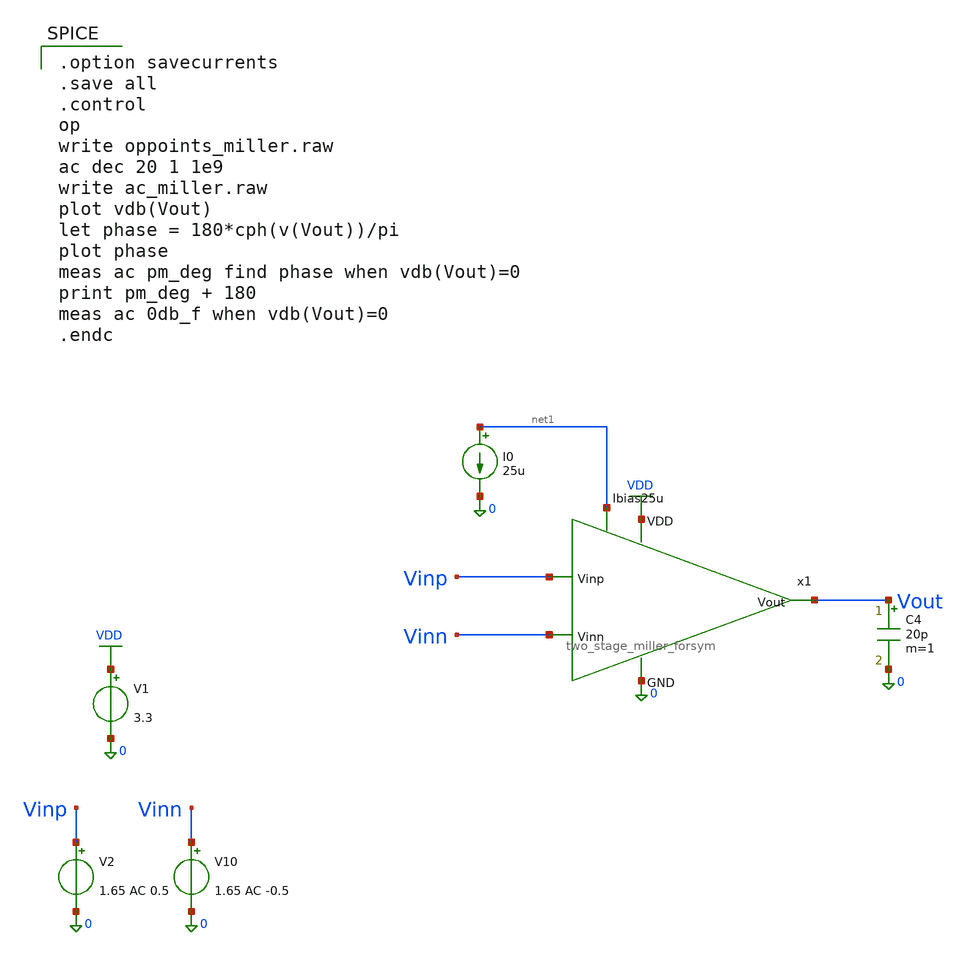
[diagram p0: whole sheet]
** sch_path: jz_tia/two_stage_miller_forsym_tb.sch
**.subckt two_stage_miller_forsym_tb
V2 Vinp 0 1.65 AC 0.5
V10 Vinn 0 1.65 AC -0.5
V1 VDD 0 3.3
I0 net1 0 25u
C4 Vout 0 20p m=1
x1 VDD Vout Vinp Vinn net1 0 two_stage_miller_forsym
**** begin user architecture code

.include $::180MCU_MODELS/design.ngspice
.lib $::180MCU_MODELS/sm141064.ngspice typical
.lib $::180MCU_MODELS/smbb000149.ngspice typical


.option savecurrents
.save all
.control
op
write oppoints_miller.raw
ac dec 20 1 1e9
write ac_miller.raw
plot vdb(Vout)
let phase = 180*cph(v(Vout))/pi
plot phase
meas ac pm_deg find phase when vdb(Vout)=0
print pm_deg + 180
meas ac 0db_f when vdb(Vout)=0
.endc

**** end user architecture code
**.ends

* expanding   symbol:  chipathon-2026-ppg/jz_tia/two_stage_miller_forsym.sym # of pins=6
** sym_path: jz_tia/xschem/two_stage_miller_forsym.sym
** sch_path: jz_tia/xschem/two_stage_miller_forsym.sch
.subckt two_stage_miller_forsym VDD Vout Vinp Vinn Ibias25u GND
*.ipin Vinn
*.ipin Vinp
*.opin Vout
*.ipin Ibias25u
*.ipin VDD
*.ipin GND
XM1 net3 net3 GND GND nfet_03v3 L=1u W=1u nf=1 ad='int((nf+1)/2) * W/nf * 0.18u' as='int((nf+2)/2) * W/nf * 0.18u'
+ pd='2*int((nf+1)/2) * (W/nf + 0.18u)' ps='2*int((nf+2)/2) * (W/nf + 0.18u)' nrd='0.18u / W' nrs='0.18u / W'
+ sa=0 sb=0 sd=0 m=1
XM2 net2 net3 GND GND nfet_03v3 L=1u W=1u nf=1 ad='int((nf+1)/2) * W/nf * 0.18u' as='int((nf+2)/2) * W/nf * 0.18u'
+ pd='2*int((nf+1)/2) * (W/nf + 0.18u)' ps='2*int((nf+2)/2) * (W/nf + 0.18u)' nrd='0.18u / W' nrs='0.18u / W'
+ sa=0 sb=0 sd=0 m=1
XM3 net1 Ibias25u VDD VDD pfet_03v3 L=1u W=14.7u nf=1 ad='int((nf+1)/2) * W/nf * 0.18u' as='int((nf+2)/2) * W/nf * 0.18u'
+ pd='2*int((nf+1)/2) * (W/nf + 0.18u)' ps='2*int((nf+2)/2) * (W/nf + 0.18u)' nrd='0.18u / W' nrs='0.18u / W'
+ sa=0 sb=0 sd=0 m=1
XM4 net3 Vinn net1 VDD pfet_03v3 L=1u W=7.4u nf=1 ad='int((nf+1)/2) * W/nf * 0.18u' as='int((nf+2)/2) * W/nf * 0.18u'
+ pd='2*int((nf+1)/2) * (W/nf + 0.18u)' ps='2*int((nf+2)/2) * (W/nf + 0.18u)' nrd='0.18u / W' nrs='0.18u / W'
+ sa=0 sb=0 sd=0 m=1
XM5 net2 Vinp net1 VDD pfet_03v3 L=1u W=7.4u nf=1 ad='int((nf+1)/2) * W/nf * 0.18u' as='int((nf+2)/2) * W/nf * 0.18u'
+ pd='2*int((nf+1)/2) * (W/nf + 0.18u)' ps='2*int((nf+2)/2) * (W/nf + 0.18u)' nrd='0.18u / W' nrs='0.18u / W'
+ sa=0 sb=0 sd=0 m=1
XM6 Vout Ibias25u VDD VDD pfet_03v3 L=0.5u W=12.1u nf=1 ad='int((nf+1)/2) * W/nf * 0.18u' as='int((nf+2)/2) * W/nf * 0.18u'
+ pd='2*int((nf+1)/2) * (W/nf + 0.18u)' ps='2*int((nf+2)/2) * (W/nf + 0.18u)' nrd='0.18u / W' nrs='0.18u / W'
+ sa=0 sb=0 sd=0 m=1
XM7 Vout net2 GND GND nfet_03v3 L=0.28u W=0.97u nf=1 ad='int((nf+1)/2) * W/nf * 0.18u' as='int((nf+2)/2) * W/nf * 0.18u'
+ pd='2*int((nf+1)/2) * (W/nf + 0.18u)' ps='2*int((nf+2)/2) * (W/nf + 0.18u)' nrd='0.18u / W' nrs='0.18u / W'
+ sa=0 sb=0 sd=0 m=1
XM8 Ibias25u Ibias25u VDD VDD pfet_03v3 L=1u W=14.7u nf=1 ad='int((nf+1)/2) * W/nf * 0.18u' as='int((nf+2)/2) * W/nf * 0.18u'
+ pd='2*int((nf+1)/2) * (W/nf + 0.18u)' ps='2*int((nf+2)/2) * (W/nf + 0.18u)' nrd='0.18u / W' nrs='0.18u / W'
+ sa=0 sb=0 sd=0 m=1
C1 net2 net4 5p m=1
R1 net4 Vout 11k m=1
.ends

.GLOBAL VDD
.end
